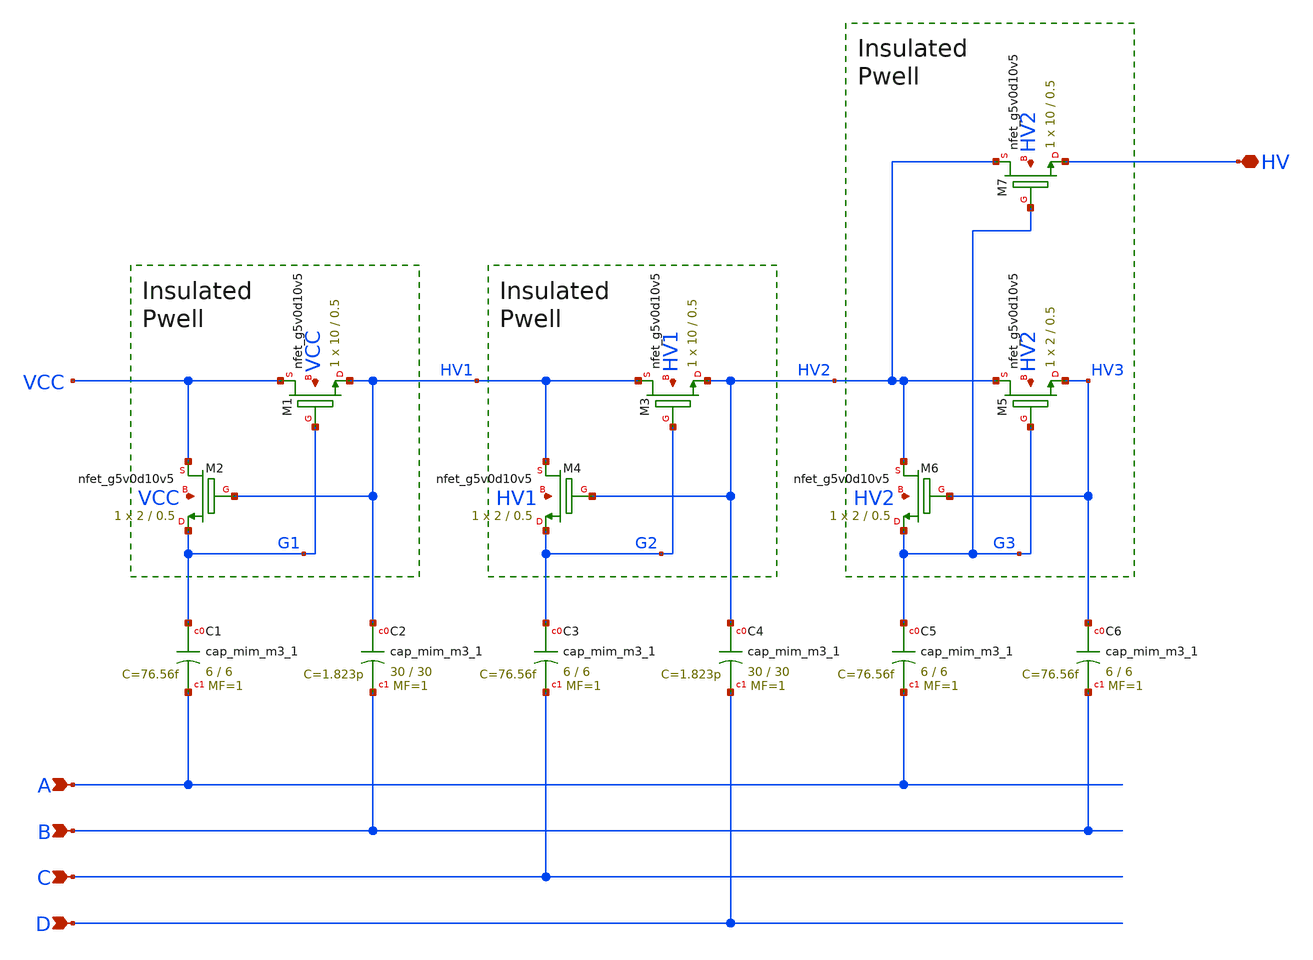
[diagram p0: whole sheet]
** sch_path: sky130_tests/charge_pump.sch
**.subckt charge_pump HV A B C D
*.iopin HV
*.ipin A
*.ipin B
*.ipin C
*.ipin D
XM1 VCC G1 HV1 VCC sky130_fd_pr__nfet_g5v0d10v5 W=10 L=0.5 ad='int((nf+1)/2) * W/nf * 0.29' pd='2*int((nf+1)/2) * (W/nf + 0.29)'
+ as='int((nf+2)/2) * W/nf * 0.29' ps='2*int((nf+2)/2) * (W/nf + 0.29)' nrd='0.29 / W' nrs='0.29 / W' sa=0
+ sb=0 sd=0 nf=1 mult=1
XM2 VCC HV1 G1 VCC sky130_fd_pr__nfet_g5v0d10v5 W=2 L=0.5 ad='int((nf+1)/2) * W/nf * 0.29' pd='2*int((nf+1)/2) * (W/nf + 0.29)'
+ as='int((nf+2)/2) * W/nf * 0.29' ps='2*int((nf+2)/2) * (W/nf + 0.29)' nrd='0.29 / W' nrs='0.29 / W' sa=0
+ sb=0 sd=0 nf=1 mult=1
XM3 HV1 G2 HV2 HV1 sky130_fd_pr__nfet_g5v0d10v5 W=10 L=0.5 ad='int((nf+1)/2) * W/nf * 0.29' pd='2*int((nf+1)/2) * (W/nf + 0.29)'
+ as='int((nf+2)/2) * W/nf * 0.29' ps='2*int((nf+2)/2) * (W/nf + 0.29)' nrd='0.29 / W' nrs='0.29 / W' sa=0
+ sb=0 sd=0 nf=1 mult=1
XM4 HV1 HV2 G2 HV1 sky130_fd_pr__nfet_g5v0d10v5 W=2 L=0.5 ad='int((nf+1)/2) * W/nf * 0.29' pd='2*int((nf+1)/2) * (W/nf + 0.29)'
+ as='int((nf+2)/2) * W/nf * 0.29' ps='2*int((nf+2)/2) * (W/nf + 0.29)' nrd='0.29 / W' nrs='0.29 / W' sa=0
+ sb=0 sd=0 nf=1 mult=1
XM5 HV2 G3 HV3 HV2 sky130_fd_pr__nfet_g5v0d10v5 W=2 L=0.5 ad='int((nf+1)/2) * W/nf * 0.29' pd='2*int((nf+1)/2) * (W/nf + 0.29)'
+ as='int((nf+2)/2) * W/nf * 0.29' ps='2*int((nf+2)/2) * (W/nf + 0.29)' nrd='0.29 / W' nrs='0.29 / W' sa=0
+ sb=0 sd=0 nf=1 mult=1
XM6 HV2 HV3 G3 HV2 sky130_fd_pr__nfet_g5v0d10v5 W=2 L=0.5 ad='int((nf+1)/2) * W/nf * 0.29' pd='2*int((nf+1)/2) * (W/nf + 0.29)'
+ as='int((nf+2)/2) * W/nf * 0.29' ps='2*int((nf+2)/2) * (W/nf + 0.29)' nrd='0.29 / W' nrs='0.29 / W' sa=0
+ sb=0 sd=0 nf=1 mult=1
XM7 HV2 G3 HV HV2 sky130_fd_pr__nfet_g5v0d10v5 W=10 L=0.5 ad='int((nf+1)/2) * W/nf * 0.29' pd='2*int((nf+1)/2) * (W/nf + 0.29)'
+ as='int((nf+2)/2) * W/nf * 0.29' ps='2*int((nf+2)/2) * (W/nf + 0.29)' nrd='0.29 / W' nrs='0.29 / W' sa=0
+ sb=0 sd=0 nf=1 mult=1
XC1 G1 A sky130_fd_pr__cap_mim_m3_1 W=6 L=6 MF=1 m=1
XC2 HV1 B sky130_fd_pr__cap_mim_m3_1 W=30 L=30 MF=1 m=1
XC3 G2 C sky130_fd_pr__cap_mim_m3_1 W=6 L=6 MF=1 m=1
XC4 HV2 D sky130_fd_pr__cap_mim_m3_1 W=30 L=30 MF=1 m=1
XC5 G3 A sky130_fd_pr__cap_mim_m3_1 W=6 L=6 MF=1 m=1
XC6 HV3 B sky130_fd_pr__cap_mim_m3_1 W=6 L=6 MF=1 m=1
**.ends
.end
